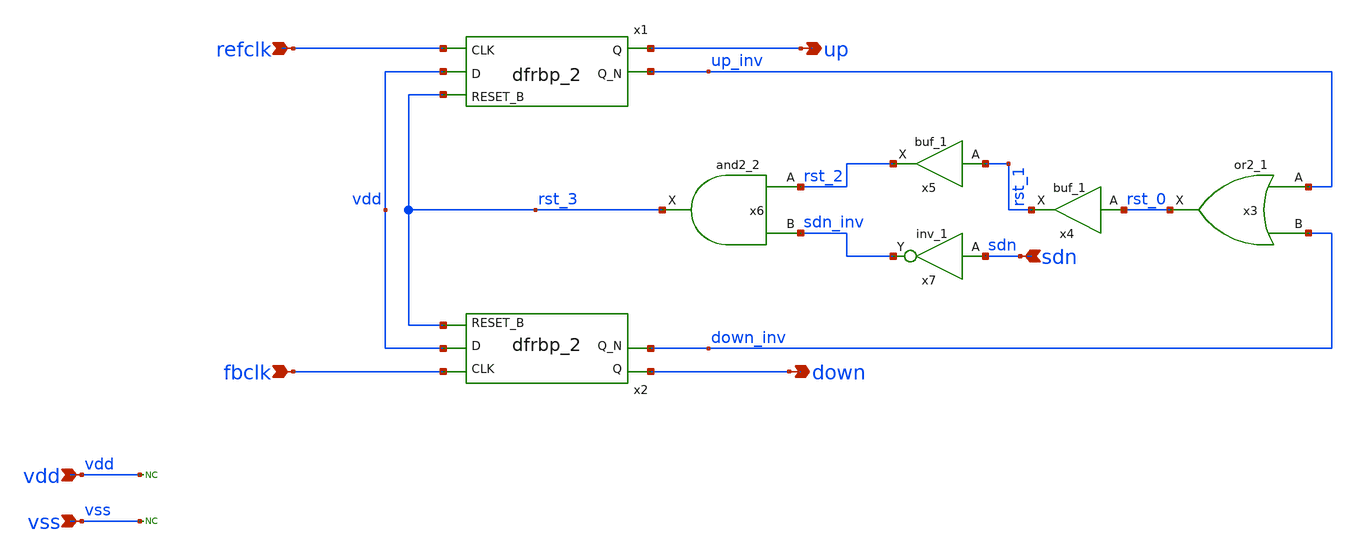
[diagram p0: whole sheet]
** sch_path: pll/pll_pfd/xschem/pll_pfd.sch
**.subckt pll_pfd refclk fbclk up down sdn vdd vss
*.ipin refclk
*.ipin fbclk
*.opin up
*.opin down
*.ipin sdn
*.ipin vdd
*.ipin vss
x1 refclk vdd rst_3 vss vss vdd vdd up up_inv sky130_fd_sc_hd__dfrbp_2
x2 fbclk vdd rst_3 vss vss vdd vdd down down_inv sky130_fd_sc_hd__dfrbp_2
x6 rst_2 sdn_inv vss vss vdd vdd rst_3 sky130_fd_sc_hd__and2_2
x4 rst_0 vss vss vdd vdd rst_1 sky130_fd_sc_hd__buf_1
x5 rst_1 vss vss vdd vdd rst_2 sky130_fd_sc_hd__buf_1
x7 sdn vss vss vdd vdd sdn_inv sky130_fd_sc_hd__inv_1
x3 up_inv down_inv vss vss vdd vdd rst_0 sky130_fd_sc_hd__or2_1
* noconn vss
* noconn vdd
**** begin user architecture code

.options wnflag=1
.include $::SKYWATER_MODELS/cells/nfet_01v8/sky130_fd_pr__nfet_01v8__tt.corner.spice
.include $::SKYWATER_MODELS/cells/nfet_01v8_lvt/sky130_fd_pr__nfet_01v8_lvt__tt.corner.spice
.include $::SKYWATER_MODELS/cells/pfet_01v8/sky130_fd_pr__pfet_01v8__tt.corner.spice
.include $::SKYWATER_MODELS/cells/nfet_03v3_nvt/sky130_fd_pr__nfet_03v3_nvt__tt.corner.spice
.include $::SKYWATER_MODELS/cells/nfet_05v0_nvt/sky130_fd_pr__nfet_05v0_nvt__tt.corner.spice
.include $::SKYWATER_MODELS/cells/esd_nfet_01v8/sky130_fd_pr__esd_nfet_01v8__tt.corner.spice
.include $::SKYWATER_MODELS/cells/pfet_01v8_lvt/sky130_fd_pr__pfet_01v8_lvt__tt.corner.spice
.include $::SKYWATER_MODELS/cells/pfet_01v8_hvt/sky130_fd_pr__pfet_01v8_hvt__tt.corner.spice
.include $::SKYWATER_MODELS/cells/esd_pfet_g5v0d10v5/sky130_fd_pr__esd_pfet_g5v0d10v5__tt.corner.spice
.include $::SKYWATER_MODELS/cells/pfet_g5v0d10v5/sky130_fd_pr__pfet_g5v0d10v5__tt.corner.spice
.include $::SKYWATER_MODELS/cells/pfet_g5v0d16v0/sky130_fd_pr__pfet_g5v0d16v0__tt.corner.spice
.include $::SKYWATER_MODELS/cells/nfet_g5v0d10v5/sky130_fd_pr__nfet_g5v0d10v5__tt.corner.spice
.include $::SKYWATER_MODELS/cells/nfet_g5v0d16v0/sky130_fd_pr__nfet_g5v0d16v0__tt_discrete.corner.spice
.include $::SKYWATER_MODELS/cells/esd_nfet_g5v0d10v5/sky130_fd_pr__esd_nfet_g5v0d10v5__tt.corner.spice
.include $::SKYWATER_MODELS/models/corners/tt/nonfet.spice

.include $::SKYWATER_MODELS/cells/cap_var_hvt/sky130_fd_pr__cap_var_hvt.model.spice

* Mismatch parameters
.include $::SKYWATER_MODELS/cells/nfet_01v8/sky130_fd_pr__nfet_01v8__mismatch.corner.spice
.include $::SKYWATER_MODELS/cells/pfet_01v8/sky130_fd_pr__pfet_01v8__mismatch.corner.spice
.include $::SKYWATER_MODELS/cells/nfet_01v8_lvt/sky130_fd_pr__nfet_01v8_lvt__mismatch.corner.spice
.include $::SKYWATER_MODELS/cells/pfet_01v8_lvt/sky130_fd_pr__pfet_01v8_lvt__mismatch.corner.spice
.include $::SKYWATER_MODELS/cells/pfet_01v8_hvt/sky130_fd_pr__pfet_01v8_hvt__mismatch.corner.spice
.include $::SKYWATER_MODELS/cells/nfet_g5v0d10v5/sky130_fd_pr__nfet_g5v0d10v5__mismatch.corner.spice
.include $::SKYWATER_MODELS/cells/pfet_g5v0d10v5/sky130_fd_pr__pfet_g5v0d10v5__mismatch.corner.spice
.include $::SKYWATER_MODELS/cells/nfet_05v0_nvt/sky130_fd_pr__nfet_05v0_nvt__mismatch.corner.spice
.include $::SKYWATER_MODELS/cells/nfet_03v3_nvt/sky130_fd_pr__nfet_03v3_nvt__mismatch.corner.spice

* Resistor$::SKYWATER_MODELS/Capacitor
.include $::SKYWATER_MODELS/models/r+c/res_typical__cap_typical.spice
.include $::SKYWATER_MODELS/models/r+c/res_typical__cap_typical__lin.spice

* Special cells
.include $::SKYWATER_MODELS/models/corners/tt/specialized_cells.spice

* All models
.include $::SKYWATER_MODELS/models/all.spice

* Corner
.include $::SKYWATER_MODELS/models/corners/tt/rf.spice

* .include $::SKYWATER_STDCELLS/cells/
.include $::SKYWATER_STDCELLS/cells/and2/sky130_fd_sc_hd__and2_1.spice
.include $::SKYWATER_STDCELLS/cells/and2/sky130_fd_sc_hd__and2_2.spice
.include $::SKYWATER_STDCELLS_HS/cells/and2/sky130_fd_sc_hs__and2_1.spice
.include $::SKYWATER_STDCELLS_HS/cells/and2/sky130_fd_sc_hs__and2_2.spice

.include $::SKYWATER_STDCELLS/cells/or2/sky130_fd_sc_hd__or2_1.spice
.include $::SKYWATER_STDCELLS/cells/or2/sky130_fd_sc_hd__or2_2.spice
.include $::SKYWATER_STDCELLS_HS/cells/or2/sky130_fd_sc_hs__or2_1.spice
.include $::SKYWATER_STDCELLS_HS/cells/or2/sky130_fd_sc_hs__or2_2.spice

.include $::SKYWATER_STDCELLS/cells/buf/sky130_fd_sc_hd__buf_1.spice
.include $::SKYWATER_STDCELLS_HS/cells/buf/sky130_fd_sc_hs__buf_1.spice

.include $::SKYWATER_STDCELLS/cells/dfrbp/sky130_fd_sc_hd__dfrbp_1.spice
.include $::SKYWATER_STDCELLS/cells/dfrbp/sky130_fd_sc_hd__dfrbp_2.spice
.include $::SKYWATER_STDCELLS_HS/cells/dfrbp/sky130_fd_sc_hs__dfrbp_1.spice
.include $::SKYWATER_STDCELLS_HS/cells/dfrbp/sky130_fd_sc_hs__dfrbp_2.spice

.include $::SKYWATER_STDCELLS/cells/inv/sky130_fd_sc_hd__inv_1.spice
.include $::SKYWATER_STDCELLS/cells/inv/sky130_fd_sc_hd__inv_2.spice
.include $::SKYWATER_STDCELLS/cells/inv/sky130_fd_sc_hd__inv_4.spice
.include $::SKYWATER_STDCELLS/cells/inv/sky130_fd_sc_hd__inv_8.spice
.include $::SKYWATER_STDCELLS/cells/inv/sky130_fd_sc_hd__inv_16.spice
.include $::SKYWATER_STDCELLS_HS/cells/inv/sky130_fd_sc_hs__inv_1.spice
.include $::SKYWATER_STDCELLS_HS/cells/inv/sky130_fd_sc_hs__inv_2.spice
.include $::SKYWATER_STDCELLS_HS/cells/inv/sky130_fd_sc_hs__inv_4.spice
.include $::SKYWATER_STDCELLS_HS/cells/inv/sky130_fd_sc_hs__inv_8.spice
.include $::SKYWATER_STDCELLS_HS/cells/inv/sky130_fd_sc_hs__inv_16.spice

.include $::SKYWATER_STDCELLS/cells/mux2/sky130_fd_sc_hd__mux2_2.spice
.include $::SKYWATER_STDCELLS/cells/nand2/sky130_fd_sc_hd__nand2_1.spice

.include $::SKYWATER_STDCELLS/cells/tap/sky130_fd_sc_hd__tap_2.spice
.include $::SKYWATER_STDCELLS/cells/tapvpwrvgnd/sky130_fd_sc_hd__tapvpwrvgnd_1.spice

**** end user architecture code
**.ends
.end
